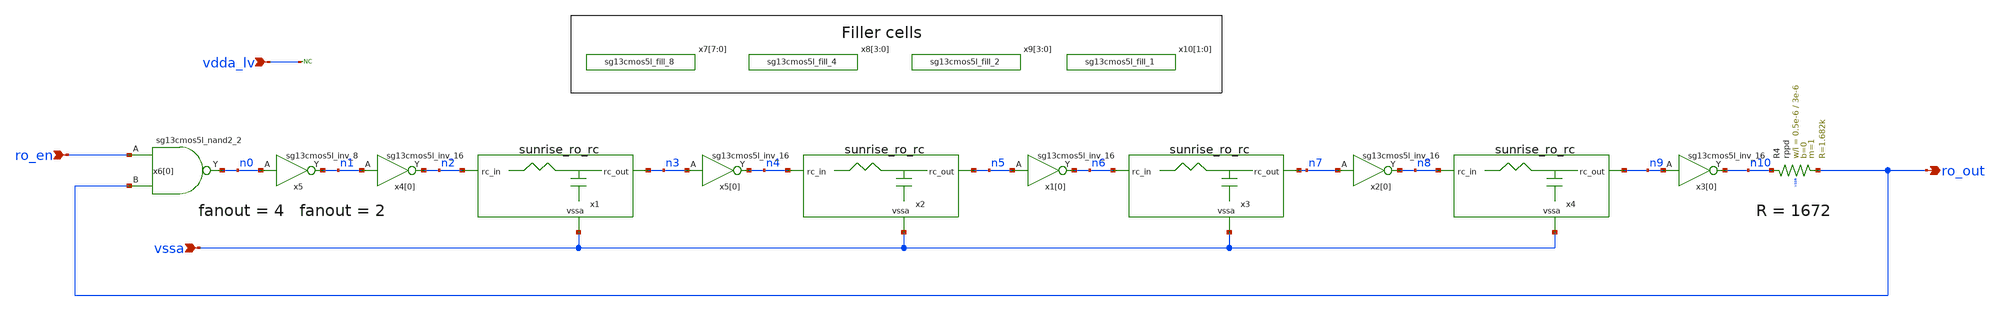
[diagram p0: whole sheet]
** sch_path: Schematics_Layout/sunrise_ro_core/sunrise_ro_core.sch
**.subckt sunrise_ro_core vdda_lv vssa ro_en ro_out
*.ipin vdda_lv
*.ipin vssa
*.ipin ro_en
*.opin ro_out
* noconn vdda_lv
XR4 n10 ro_out vssa rppd w=0.5e-6 l=3e-6 m=1 b=0 mm_ok=1
x1 n3 n2 vssa sunrise_ro_rc
x2 n5 n4 vssa sunrise_ro_rc
x3 n7 n6 vssa sunrise_ro_rc
x4 n9 n8 vssa sunrise_ro_rc
x6[0] n0 ro_en ro_out vdda_lv vssa sg13cmos5l_nand2_2
x5[0] n4 n3 vdda_lv vssa sg13cmos5l_inv_16
x1[0] n6 n5 vdda_lv vssa sg13cmos5l_inv_16
x2[0] n8 n7 vdda_lv vssa sg13cmos5l_inv_16
x3[0] n10 n9 vdda_lv vssa sg13cmos5l_inv_16
x5 n1 n0 vdda_lv vssa sg13cmos5l_inv_8
x4[0] n2 n1 vdda_lv vssa sg13cmos5l_inv_16
x7[7] vdda_lv vssa sg13cmos5l_fill_8
x7[6] vdda_lv vssa sg13cmos5l_fill_8
x7[5] vdda_lv vssa sg13cmos5l_fill_8
x7[4] vdda_lv vssa sg13cmos5l_fill_8
x7[3] vdda_lv vssa sg13cmos5l_fill_8
x7[2] vdda_lv vssa sg13cmos5l_fill_8
x7[1] vdda_lv vssa sg13cmos5l_fill_8
x7[0] vdda_lv vssa sg13cmos5l_fill_8
x8[3] vdda_lv vssa sg13cmos5l_fill_4
x8[2] vdda_lv vssa sg13cmos5l_fill_4
x8[1] vdda_lv vssa sg13cmos5l_fill_4
x8[0] vdda_lv vssa sg13cmos5l_fill_4
x9[3] vdda_lv vssa sg13cmos5l_fill_2
x9[2] vdda_lv vssa sg13cmos5l_fill_2
x9[1] vdda_lv vssa sg13cmos5l_fill_2
x9[0] vdda_lv vssa sg13cmos5l_fill_2
x10[1] vdda_lv vssa sg13cmos5l_fill_1
x10[0] vdda_lv vssa sg13cmos5l_fill_1
**.ends
.end
